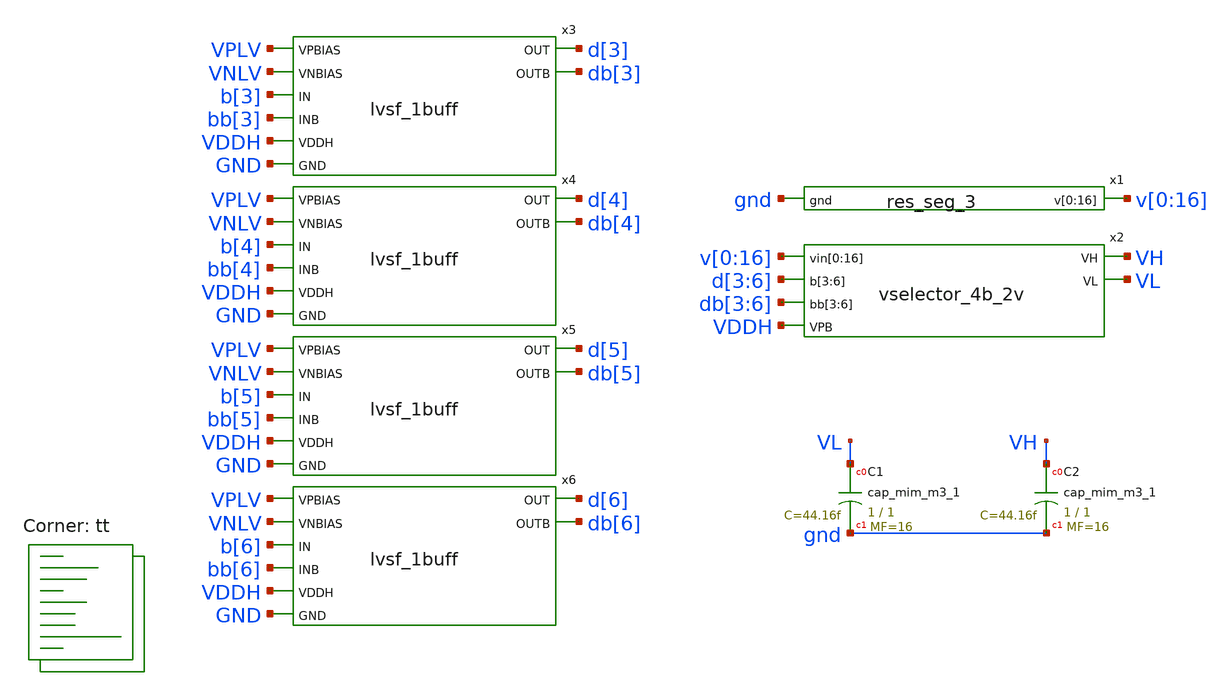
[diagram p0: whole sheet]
** sch_path: xschem/res_seg_3-tb.sch
**.subckt res_seg_3-tb
x1 v[0] v[1] v[2] v[3] v[4] v[5] v[6] v[7] v[8] v[9] v[10] v[11] v[12] v[13] v[14] v[15] v[16] gnd
+ res_seg_3
XC1 VL gnd sky130_fd_pr__cap_mim_m3_1 W=1 L=1 MF=16 m=16
XC2 VH gnd sky130_fd_pr__cap_mim_m3_1 W=1 L=1 MF=16 m=16
x2 v[0] v[1] v[2] v[3] v[4] v[5] v[6] v[7] v[8] v[9] v[10] v[11] v[12] v[13] v[14] v[15] v[16] d[3]
+ d[4] d[5] d[6] db[3] db[4] db[5] db[6] VH VL VDDH vselector_4b_2v
x3 VPLV VNLV b[3] bb[3] d[3] db[3] VDDH GND lvsf_1buff
x4 VPLV VNLV b[4] bb[4] d[4] db[4] VDDH GND lvsf_1buff
x5 VPLV VNLV b[5] bb[5] d[5] db[5] VDDH GND lvsf_1buff
x6 VPLV VNLV b[6] bb[6] d[6] db[6] VDDH GND lvsf_1buff
**** begin user architecture code



  .option wnflag=1
  .option safecurrents
  ********************Static Voltage Sources***************************
  Vddh vddh gnd dc 5.5
  Vpb  vpb  gnd dc 5.5

  .param vpb_val = 2.98 vnb_val=1.506
  Vp vpbias gnd dc vpb_val
  Vn vnbias gnd dc vnb_val

  vpblv vplv gnd 3.6965
  vnblv vnlv gnd 1.354

  V16 v[16] gnd dc 4.7190
  v0 v[0] gnd dc 4.0164
  ********************Dynamic Voltage Sources***************************
  *******Calculation**********
  .param base_f=100e3 base_t={1/base_f} base_th={base_t/2} base_d={base_th}
  .param b3_th={base_th} b3_t={b3_th*2}
  .param b4_th={b3_th*2} b4_t={b4_th*2}
  .param b5_th={b4_th*2} b5_t={b5_th*2}
  .param b6_th={b5_th*2} b6_t={b6_th*2}
  *******Signals**********
  .param vhi=1.8
  Vb3  b[3]  gnd pulse({vhi} 0 {base_d} 1n 1n {b3_th} {b3_t})
  Vb4  b[4]  gnd pulse({vhi} 0 {base_d} 1n 1n {b4_th} {b4_t})
  Vb5  b[5]  gnd pulse({vhi} 0 {base_d} 1n 1n {b5_th} {b5_t})
  Vb6  b[6]  gnd pulse({vhi} 0 {base_d} 1n 1n {b6_th} {b6_t})

  Vbb3  bb[3]  gnd pulse(0 {vhi} {base_d} 1n 1n {b3_th} {b3_t})
  Vbb4  bb[4]  gnd pulse(0 {vhi} {base_d} 1n 1n {b4_th} {b4_t})
  Vbb5  bb[5]  gnd pulse(0 {vhi} {base_d} 1n 1n {b5_th} {b5_t})
  Vbb6  bb[6]  gnd pulse(0 {vhi} {base_d} 1n 1n {b6_th} {b6_t})
  ********************Simulation Commands*****************************
  .control
     reset
     save all
     tran 1n 100u
     write res_seg_3-tb.raw
     set appendwrite
*    quit 0
  .endc



.lib $::SKYWATER_MODELS/sky130.lib.spice tt
**** end user architecture code
**.ends

* expanding   symbol:  res_seg_3.sym # of pins=2
** sym_path: xschem/res_seg_3.sym
** sch_path: xschem/res_seg_3.sch
.subckt res_seg_3 v[0] v[1] v[2] v[3] v[4] v[5] v[6] v[7] v[8] v[9] v[10] v[11] v[12] v[13] v[14]
+ v[15] v[16] gnd
*.opin v[0],v[1],v[2],v[3],v[4],v[5],v[6],v[7],v[8],v[9],v[10],v[11],v[12],v[13],v[14],v[15],v[16]
*.ipin gnd
XR1 v[0] v[1] gnd sky130_fd_pr__res_xhigh_po_0p35 L=0.5555 mult=1 m=1
XR2 v[1] v[2] gnd sky130_fd_pr__res_xhigh_po_0p35 L=0.5726 mult=1 m=1
XR3 v[2] v[3] gnd sky130_fd_pr__res_xhigh_po_0p35 L=0.5811 mult=1 m=1
XR4 v[3] v[4] gnd sky130_fd_pr__res_xhigh_po_0p35 L=0.5897 mult=1 m=1
XR5 v[4] v[5] gnd sky130_fd_pr__res_xhigh_po_0p35 L=0.6153 mult=1 m=1
XR6 v[5] v[6] gnd sky130_fd_pr__res_xhigh_po_0p35 L=0.6238 mult=1 m=1
XR7 v[6] v[7] gnd sky130_fd_pr__res_xhigh_po_0p35 L=0.6409 mult=1 m=1
XR8 v[7] v[8] gnd sky130_fd_pr__res_xhigh_po_0p35 L=0.6666 mult=1 m=1
XR9 v[8] v[9] gnd sky130_fd_pr__res_xhigh_po_0p35 L=0.6837 mult=1 m=1
XR10 v[9] v[10] gnd sky130_fd_pr__res_xhigh_po_0p35 L=0.7093 mult=1 m=1
XR11 v[10] v[11] gnd sky130_fd_pr__res_xhigh_po_0p35 L=0.7264 mult=1 m=1
XR12 v[11] v[12] gnd sky130_fd_pr__res_xhigh_po_0p35 L=0.7691 mult=1 m=1
XR13 v[12] v[13] gnd sky130_fd_pr__res_xhigh_po_0p35 L=0.7948 mult=1 m=1
XR14 v[13] v[14] gnd sky130_fd_pr__res_xhigh_po_0p35 L=0.8375 mult=1 m=1
XR15 v[14] v[15] gnd sky130_fd_pr__res_xhigh_po_0p35 L=0.8802 mult=1 m=1
XR16 v[15] v[16] gnd sky130_fd_pr__res_xhigh_po_0p35 L=0.9315 mult=1 m=1
.ends


* expanding   symbol:  vselector_4b_2v.sym # of pins=6
** sym_path: xschem/vselector_4b_2v.sym
** sch_path: xschem/vselector_4b_2v.sch
.subckt vselector_4b_2v vin[0] vin[1] vin[2] vin[3] vin[4] vin[5] vin[6] vin[7] vin[8] vin[9]
+ vin[10] vin[11] vin[12] vin[13] vin[14] vin[15] vin[16] b[3] b[4] b[5] b[6] bb[3] bb[4] bb[5] bb[6] VH VL
+ VPB
*.ipin
*+ vin[0],vin[1],vin[2],vin[3],vin[4],vin[5],vin[6],vin[7],vin[8],vin[9],vin[10],vin[11],vin[12],vin[13],vin[14],vin[15],vin[16]
*.opin VH
*.ipin VPB
*.ipin b[3],b[4],b[5],b[6]
*.opin VL
*.ipin bb[3],bb[4],bb[5],bb[6]
x1 vin[0] vin[1] vin[2] vin[3] vin[4] vin[5] vin[6] vin[7] vin[8] b[6] v1[0] v1[1] v1[2] v1[3] v1[4]
+ v1[5] v1[6] v1[7] v1[8] VPB switch_pmos_1g_9o
x2 vin[8] vin[9] vin[10] vin[11] vin[12] vin[13] vin[14] vin[15] vin[16] bb[6] v1[0] v1[1] v1[2]
+ v1[3] v1[4] v1[5] v1[6] v1[7] v1[8] VPB switch_pmos_1g_9o
x3 v1[0] v1[1] v1[2] v1[3] v1[4] b[5] v2[0] v2[1] v2[2] v2[3] v2[4] VPB switch_pmos_1g_5o
x4 v1[4] v1[5] v1[6] v1[7] v1[8] bb[5] v2[0] v2[1] v2[2] v2[3] v2[4] VPB switch_pmos_1g_5o
x5 v2[0] v2[1] v2[2] b[4] v3[0] v3[1] v3[2] VPB switch_pmos_1g_3o
x6 v2[2] v2[3] v2[4] bb[4] v3[0] v3[1] v3[2] VPB switch_pmos_1g_3o
x7 v3[0] v3[1] b[3] VH VL VPB switch_pmos_1g_2o
x8 v3[1] v3[2] bb[3] VH VL VPB switch_pmos_1g_2o
.ends


* expanding   symbol:  lvsf_1buff.sym # of pins=8
** sym_path: xschem/lvsf_1buff.sym
** sch_path: xschem/lvsf_1buff.sch
.subckt lvsf_1buff VPBIAS VNBIAS IN INB OUT OUTB VDDH GND
*.ipin IN
*.ipin INB
*.opin OUT
*.ipin VDDH
*.ipin GND
*.ipin VPBIAS
*.ipin VNBIAS
*.opin OUTB
Vmeas net1 net2 0
.save i(vmeas)
XM13 net6 IN GND GND sky130_fd_pr__nfet_01v8 L=0.15 W=3 nf=1 ad='int((nf+1)/2) * W/nf * 0.29' as='int((nf+2)/2) * W/nf * 0.29'
+ pd='2*int((nf+1)/2) * (W/nf + 0.29)' ps='2*int((nf+2)/2) * (W/nf + 0.29)' nrd='0.29 / W' nrs='0.29 / W'
+ sa=0 sb=0 sd=0 mult=1 m=1
XM1 net3 VPBIAS VDDH VDDH sky130_fd_pr__pfet_g5v0d10v5 L=0.8 W=1 nf=1 ad='int((nf+1)/2) * W/nf * 0.29'
+ as='int((nf+2)/2) * W/nf * 0.29' pd='2*int((nf+1)/2) * (W/nf + 0.29)' ps='2*int((nf+2)/2) * (W/nf + 0.29)'
+ nrd='0.29 / W' nrs='0.29 / W' sa=0 sb=0 sd=0 mult=1 m=1
XM2 net1 VPBIAS VDDH VDDH sky130_fd_pr__pfet_g5v0d10v5 L=0.8 W=1 nf=1 ad='int((nf+1)/2) * W/nf * 0.29'
+ as='int((nf+2)/2) * W/nf * 0.29' pd='2*int((nf+1)/2) * (W/nf + 0.29)' ps='2*int((nf+2)/2) * (W/nf + 0.29)'
+ nrd='0.29 / W' nrs='0.29 / W' sa=0 sb=0 sd=0 mult=1 m=1
XM3 OUTPB OUTP net4 VDDH sky130_fd_pr__pfet_g5v0d10v5 L=0.8 W=1 nf=1 ad='int((nf+1)/2) * W/nf * 0.29'
+ as='int((nf+2)/2) * W/nf * 0.29' pd='2*int((nf+1)/2) * (W/nf + 0.29)' ps='2*int((nf+2)/2) * (W/nf + 0.29)'
+ nrd='0.29 / W' nrs='0.29 / W' sa=0 sb=0 sd=0 mult=1 m=1
XM4 OUTP OUTPB net2 VDDH sky130_fd_pr__pfet_g5v0d10v5 L=0.8 W=1 nf=1 ad='int((nf+1)/2) * W/nf * 0.29'
+ as='int((nf+2)/2) * W/nf * 0.29' pd='2*int((nf+1)/2) * (W/nf + 0.29)' ps='2*int((nf+2)/2) * (W/nf + 0.29)'
+ nrd='0.29 / W' nrs='0.29 / W' sa=0 sb=0 sd=0 mult=1 m=1
XM5 OUTPB VNBIAS n1 GND sky130_fd_pr__nfet_g5v0d10v5 L=1 W=1 nf=1 ad='int((nf+1)/2) * W/nf * 0.29' as='int((nf+2)/2) * W/nf * 0.29'
+ pd='2*int((nf+1)/2) * (W/nf + 0.29)' ps='2*int((nf+2)/2) * (W/nf + 0.29)' nrd='0.29 / W' nrs='0.29 / W'
+ sa=0 sb=0 sd=0 mult=1 m=1
XM6 OUTP VNBIAS n2 GND sky130_fd_pr__nfet_g5v0d10v5 L=1 W=1 nf=1 ad='int((nf+1)/2) * W/nf * 0.29' as='int((nf+2)/2) * W/nf * 0.29'
+ pd='2*int((nf+1)/2) * (W/nf + 0.29)' ps='2*int((nf+2)/2) * (W/nf + 0.29)' nrd='0.29 / W' nrs='0.29 / W'
+ sa=0 sb=0 sd=0 mult=1 m=1
Vmeas1 net3 net4 0
.save i(vmeas1)
XM7 net5 INB GND GND sky130_fd_pr__nfet_01v8 L=0.15 W=3 nf=1 ad='int((nf+1)/2) * W/nf * 0.29' as='int((nf+2)/2) * W/nf * 0.29'
+ pd='2*int((nf+1)/2) * (W/nf + 0.29)' ps='2*int((nf+2)/2) * (W/nf + 0.29)' nrd='0.29 / W' nrs='0.29 / W'
+ sa=0 sb=0 sd=0 mult=1 m=1
Vmeas2 n2 net5 0
.save i(vmeas2)
Vmeas3 n1 net6 0
.save i(vmeas3)
x1 OUTP OUTB VDDH GND inv_hvl m=1
x2 OUTB OUT VDDH GND inv_hvl m=1
.ends


* expanding   symbol:  switch_pmos_1g_9o.sym # of pins=4
** sym_path: xschem/switch_pmos_1g_9o.sym
** sch_path: xschem/switch_pmos_1g_9o.sch
.subckt switch_pmos_1g_9o vin[0] vin[1] vin[2] vin[3] vin[4] vin[5] vin[6] vin[7] vin[8] DIN vout[0]
+ vout[1] vout[2] vout[3] vout[4] vout[5] vout[6] vout[7] vout[8] VPB
*.ipin vin[0],vin[1],vin[2],vin[3],vin[4],vin[5],vin[6],vin[7],vin[8]
*.opin vout[0],vout[1],vout[2],vout[3],vout[4],vout[5],vout[6],vout[7],vout[8]
*.ipin VPB
*.ipin DIN
.param wp=0.42 wn=0.42 l=0.5

XM1 vout[0] DIN vin[0] VPB sky130_fd_pr__pfet_g5v0d10v5 L=l W=wp nf=1 ad='int((nf+1)/2) * W/nf * 0.29'
+ as='int((nf+2)/2) * W/nf * 0.29' pd='2*int((nf+1)/2) * (W/nf + 0.29)' ps='2*int((nf+2)/2) * (W/nf + 0.29)'
+ nrd='0.29 / W' nrs='0.29 / W' sa=0 sb=0 sd=0 mult=1 m=1
XM2 vout[1] DIN vin[1] VPB sky130_fd_pr__pfet_g5v0d10v5 L=l W=wp nf=1 ad='int((nf+1)/2) * W/nf * 0.29'
+ as='int((nf+2)/2) * W/nf * 0.29' pd='2*int((nf+1)/2) * (W/nf + 0.29)' ps='2*int((nf+2)/2) * (W/nf + 0.29)'
+ nrd='0.29 / W' nrs='0.29 / W' sa=0 sb=0 sd=0 mult=1 m=1
XM3 vout[2] DIN vin[2] VPB sky130_fd_pr__pfet_g5v0d10v5 L=l W=wp nf=1 ad='int((nf+1)/2) * W/nf * 0.29'
+ as='int((nf+2)/2) * W/nf * 0.29' pd='2*int((nf+1)/2) * (W/nf + 0.29)' ps='2*int((nf+2)/2) * (W/nf + 0.29)'
+ nrd='0.29 / W' nrs='0.29 / W' sa=0 sb=0 sd=0 mult=1 m=1
XM4 vout[3] DIN vin[3] VPB sky130_fd_pr__pfet_g5v0d10v5 L=l W=wp nf=1 ad='int((nf+1)/2) * W/nf * 0.29'
+ as='int((nf+2)/2) * W/nf * 0.29' pd='2*int((nf+1)/2) * (W/nf + 0.29)' ps='2*int((nf+2)/2) * (W/nf + 0.29)'
+ nrd='0.29 / W' nrs='0.29 / W' sa=0 sb=0 sd=0 mult=1 m=1
XM5 vout[4] DIN vin[4] VPB sky130_fd_pr__pfet_g5v0d10v5 L=l W=wp nf=1 ad='int((nf+1)/2) * W/nf * 0.29'
+ as='int((nf+2)/2) * W/nf * 0.29' pd='2*int((nf+1)/2) * (W/nf + 0.29)' ps='2*int((nf+2)/2) * (W/nf + 0.29)'
+ nrd='0.29 / W' nrs='0.29 / W' sa=0 sb=0 sd=0 mult=1 m=1
XM6 vout[5] DIN vin[5] VPB sky130_fd_pr__pfet_g5v0d10v5 L=l W=wp nf=1 ad='int((nf+1)/2) * W/nf * 0.29'
+ as='int((nf+2)/2) * W/nf * 0.29' pd='2*int((nf+1)/2) * (W/nf + 0.29)' ps='2*int((nf+2)/2) * (W/nf + 0.29)'
+ nrd='0.29 / W' nrs='0.29 / W' sa=0 sb=0 sd=0 mult=1 m=1
XM7 vout[6] DIN vin[6] VPB sky130_fd_pr__pfet_g5v0d10v5 L=l W=wp nf=1 ad='int((nf+1)/2) * W/nf * 0.29'
+ as='int((nf+2)/2) * W/nf * 0.29' pd='2*int((nf+1)/2) * (W/nf + 0.29)' ps='2*int((nf+2)/2) * (W/nf + 0.29)'
+ nrd='0.29 / W' nrs='0.29 / W' sa=0 sb=0 sd=0 mult=1 m=1
XM8 vout[7] DIN vin[7] VPB sky130_fd_pr__pfet_g5v0d10v5 L=l W=wp nf=1 ad='int((nf+1)/2) * W/nf * 0.29'
+ as='int((nf+2)/2) * W/nf * 0.29' pd='2*int((nf+1)/2) * (W/nf + 0.29)' ps='2*int((nf+2)/2) * (W/nf + 0.29)'
+ nrd='0.29 / W' nrs='0.29 / W' sa=0 sb=0 sd=0 mult=1 m=1
XM9 vout[8] DIN vin[8] VPB sky130_fd_pr__pfet_g5v0d10v5 L=l W=wp nf=1 ad='int((nf+1)/2) * W/nf * 0.29'
+ as='int((nf+2)/2) * W/nf * 0.29' pd='2*int((nf+1)/2) * (W/nf + 0.29)' ps='2*int((nf+2)/2) * (W/nf + 0.29)'
+ nrd='0.29 / W' nrs='0.29 / W' sa=0 sb=0 sd=0 mult=1 m=1
.ends


* expanding   symbol:  switch_pmos_1g_5o.sym # of pins=4
** sym_path: xschem/switch_pmos_1g_5o.sym
** sch_path: xschem/switch_pmos_1g_5o.sch
.subckt switch_pmos_1g_5o vin[0] vin[1] vin[2] vin[3] vin[4] DIN vout[0] vout[1] vout[2] vout[3]
+ vout[4] VPB
*.ipin vin[0],vin[1],vin[2],vin[3],vin[4]
*.opin vout[0],vout[1],vout[2],vout[3],vout[4]
*.ipin VPB
*.ipin DIN
.param wp=0.42 wn=0.42 l=0.5

XM1 vout[0] DIN vin[0] VPB sky130_fd_pr__pfet_g5v0d10v5 L=l W=wp nf=1 ad='int((nf+1)/2) * W/nf * 0.29'
+ as='int((nf+2)/2) * W/nf * 0.29' pd='2*int((nf+1)/2) * (W/nf + 0.29)' ps='2*int((nf+2)/2) * (W/nf + 0.29)'
+ nrd='0.29 / W' nrs='0.29 / W' sa=0 sb=0 sd=0 mult=1 m=1
XM2 vout[1] DIN vin[1] VPB sky130_fd_pr__pfet_g5v0d10v5 L=l W=wp nf=1 ad='int((nf+1)/2) * W/nf * 0.29'
+ as='int((nf+2)/2) * W/nf * 0.29' pd='2*int((nf+1)/2) * (W/nf + 0.29)' ps='2*int((nf+2)/2) * (W/nf + 0.29)'
+ nrd='0.29 / W' nrs='0.29 / W' sa=0 sb=0 sd=0 mult=1 m=1
XM3 vout[2] DIN vin[2] VPB sky130_fd_pr__pfet_g5v0d10v5 L=l W=wp nf=1 ad='int((nf+1)/2) * W/nf * 0.29'
+ as='int((nf+2)/2) * W/nf * 0.29' pd='2*int((nf+1)/2) * (W/nf + 0.29)' ps='2*int((nf+2)/2) * (W/nf + 0.29)'
+ nrd='0.29 / W' nrs='0.29 / W' sa=0 sb=0 sd=0 mult=1 m=1
XM4 vout[3] DIN vin[3] VPB sky130_fd_pr__pfet_g5v0d10v5 L=l W=wp nf=1 ad='int((nf+1)/2) * W/nf * 0.29'
+ as='int((nf+2)/2) * W/nf * 0.29' pd='2*int((nf+1)/2) * (W/nf + 0.29)' ps='2*int((nf+2)/2) * (W/nf + 0.29)'
+ nrd='0.29 / W' nrs='0.29 / W' sa=0 sb=0 sd=0 mult=1 m=1
XM5 vout[4] DIN vin[4] VPB sky130_fd_pr__pfet_g5v0d10v5 L=l W=wp nf=1 ad='int((nf+1)/2) * W/nf * 0.29'
+ as='int((nf+2)/2) * W/nf * 0.29' pd='2*int((nf+1)/2) * (W/nf + 0.29)' ps='2*int((nf+2)/2) * (W/nf + 0.29)'
+ nrd='0.29 / W' nrs='0.29 / W' sa=0 sb=0 sd=0 mult=1 m=1
.ends


* expanding   symbol:  switch_pmos_1g_3o.sym # of pins=4
** sym_path: xschem/switch_pmos_1g_3o.sym
** sch_path: xschem/switch_pmos_1g_3o.sch
.subckt switch_pmos_1g_3o vin[0] vin[1] vin[2] DIN vout[0] vout[1] vout[2] VPB
*.ipin vin[0],vin[1],vin[2]
*.opin vout[0],vout[1],vout[2]
*.ipin VPB
*.ipin DIN
.param wp=0.42 wn=0.42 l=0.5

XM1 vout[0] DIN vin[0] VPB sky130_fd_pr__pfet_g5v0d10v5 L=l W=wp nf=1 ad='int((nf+1)/2) * W/nf * 0.29'
+ as='int((nf+2)/2) * W/nf * 0.29' pd='2*int((nf+1)/2) * (W/nf + 0.29)' ps='2*int((nf+2)/2) * (W/nf + 0.29)'
+ nrd='0.29 / W' nrs='0.29 / W' sa=0 sb=0 sd=0 mult=1 m=1
XM2 vout[1] DIN vin[1] VPB sky130_fd_pr__pfet_g5v0d10v5 L=l W=wp nf=1 ad='int((nf+1)/2) * W/nf * 0.29'
+ as='int((nf+2)/2) * W/nf * 0.29' pd='2*int((nf+1)/2) * (W/nf + 0.29)' ps='2*int((nf+2)/2) * (W/nf + 0.29)'
+ nrd='0.29 / W' nrs='0.29 / W' sa=0 sb=0 sd=0 mult=1 m=1
XM3 vout[2] DIN vin[2] VPB sky130_fd_pr__pfet_g5v0d10v5 L=l W=wp nf=1 ad='int((nf+1)/2) * W/nf * 0.29'
+ as='int((nf+2)/2) * W/nf * 0.29' pd='2*int((nf+1)/2) * (W/nf + 0.29)' ps='2*int((nf+2)/2) * (W/nf + 0.29)'
+ nrd='0.29 / W' nrs='0.29 / W' sa=0 sb=0 sd=0 mult=1 m=1
.ends


* expanding   symbol:  switch_pmos_1g_2o.sym # of pins=5
** sym_path: xschem/switch_pmos_1g_2o.sym
** sch_path: xschem/switch_pmos_1g_2o.sch
.subckt switch_pmos_1g_2o vin[0] vin[1] DIN VH VL VPB
*.ipin vin[0],vin[1]
*.opin VH
*.ipin VPB
*.ipin DIN
*.opin VL
.param wp=0.42 wn=0.42 l=0.5

XM1 VL DIN vin[0] VPB sky130_fd_pr__pfet_g5v0d10v5 L=l W=wp nf=1 ad='int((nf+1)/2) * W/nf * 0.29' as='int((nf+2)/2) * W/nf * 0.29'
+ pd='2*int((nf+1)/2) * (W/nf + 0.29)' ps='2*int((nf+2)/2) * (W/nf + 0.29)' nrd='0.29 / W' nrs='0.29 / W'
+ sa=0 sb=0 sd=0 mult=1 m=1
XM2 VH DIN vin[1] VPB sky130_fd_pr__pfet_g5v0d10v5 L=l W=wp nf=1 ad='int((nf+1)/2) * W/nf * 0.29' as='int((nf+2)/2) * W/nf * 0.29'
+ pd='2*int((nf+1)/2) * (W/nf + 0.29)' ps='2*int((nf+2)/2) * (W/nf + 0.29)' nrd='0.29 / W' nrs='0.29 / W'
+ sa=0 sb=0 sd=0 mult=1 m=1
.ends


* expanding   symbol:  inv_hvl.sym # of pins=4
** sym_path: xschem/inv_hvl.sym
** sch_path: xschem/inv_hvl.sch
.subckt inv_hvl in out VDDH GND
*.opin out
*.ipin VDDH
*.ipin GND
*.ipin in
.param wp=0.84 wn=0.42 l=0.5
XM1 out in VDDH VDDH sky130_fd_pr__pfet_g5v0d10v5 L=l W=wp nf=1 ad='int((nf+1)/2) * W/nf * 0.29' as='int((nf+2)/2) * W/nf * 0.29'
+ pd='2*int((nf+1)/2) * (W/nf + 0.29)' ps='2*int((nf+2)/2) * (W/nf + 0.29)' nrd='0.29 / W' nrs='0.29 / W'
+ sa=0 sb=0 sd=0 mult=m m=m
XM2 out in GND GND sky130_fd_pr__nfet_g5v0d10v5 L=l W=wn nf=1 ad='int((nf+1)/2) * W/nf * 0.29' as='int((nf+2)/2) * W/nf * 0.29'
+ pd='2*int((nf+1)/2) * (W/nf + 0.29)' ps='2*int((nf+2)/2) * (W/nf + 0.29)' nrd='0.29 / W' nrs='0.29 / W'
+ sa=0 sb=0 sd=0 mult=m m=m
.ends

.end
